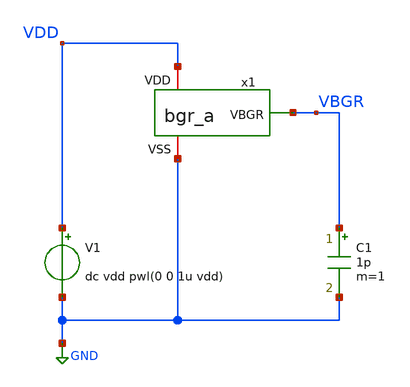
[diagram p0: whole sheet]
** sch_path: member_project/BGR/Maehashi/design/tb_bgr_a.sch
**.subckt tb_bgr_a
x1 VDD VBGR GND bgr_a
V1 VDD GND dc vdd pwl(0 0 1u vdd)
C1 VBGR GND 1p m=1
**** begin user architecture code


.option savecurrents
.temp 40
.param vdd = 5
.control
set units=degree
save all

alterparam vthMN = 0.1 ; Slow:0.1, Fast:-0.1
alterparam vthMP = 0.1 ; Slow:-0.1, Fast:0.1
alterparam magRS = 1 ; Slow:1.2, Fast:0.85
reset

op
show m
let vsat_marg_mp1 = @m.x1.xxmp1.m1[vds] - (@m.x1.xxmp1.m1[vgs] - @m.x1.xxmp1.m1[vth])
let vsat_marg_mp2 = @m.x1.xxmp2.m1[vds] - (@m.x1.xxmp2.m1[vgs] - @m.x1.xxmp2.m1[vth])
let vsat_marg_mp3 = @m.x1.xxmp3.m1[vds] - (@m.x1.xxmp3.m1[vgs] - @m.x1.xxmp3.m1[vth])
let vsat_marg_mp4 = @m.x1.xxmp4.m1[vds] - (@m.x1.xxmp4.m1[vgs] - @m.x1.xxmp4.m1[vth])
let vsat_marg_mp5 = @m.x1.xxmp5.m1[vds] - (@m.x1.xxmp5.m1[vgs] - @m.x1.xxmp5.m1[vth])
let vsat_marg_mp6 = @m.x1.xxmp6.m1[vds] - (@m.x1.xxmp6.m1[vgs] - @m.x1.xxmp6.m1[vth])

let vsat_marg_mn1 = @m.x1.xxmn1.m1[vds] - (@m.x1.xxmn1.m1[vgs] - @m.x1.xxmn1.m1[vth])
let vsat_marg_mn2 = @m.x1.xxmn2.m1[vds] - (@m.x1.xxmn2.m1[vgs] - @m.x1.xxmn2.m1[vth])
let vsat_marg_mn3 = @m.x1.xxmn3.m1[vds] - (@m.x1.xxmn3.m1[vgs] - @m.x1.xxmn3.m1[vth])
let vsat_marg_mn4 = @m.x1.xxmn4.m1[vds] - (@m.x1.xxmn4.m1[vgs] - @m.x1.xxmn4.m1[vth])

*echo '*** SF/5.0V/40deg ***' >> bgr_a_dcop.txt
*echo 'ignore VsatMargin Vds Vgs Vth' >> bgr_a_dcop.txt
*set appendwrite
*set wr_singlescale
*wrdata bgr_a_dcop.txt vsat_marg_mp1 @m.x1.xxmp1.m1[vds] @m.x1.xxmp1.m1[vgs] @m.x1.xxmp1.m1[vth]
*wrdata bgr_a_dcop.txt vsat_marg_mp2 @m.x1.xxmp2.m1[vds] @m.x1.xxmp2.m1[vgs] @m.x1.xxmp2.m1[vth]
*wrdata bgr_a_dcop.txt vsat_marg_mp3 @m.x1.xxmp3.m1[vds] @m.x1.xxmp3.m1[vgs] @m.x1.xxmp3.m1[vth]
*wrdata bgr_a_dcop.txt vsat_marg_mp4 @m.x1.xxmp4.m1[vds] @m.x1.xxmp4.m1[vgs] @m.x1.xxmp4.m1[vth]
*wrdata bgr_a_dcop.txt vsat_marg_mp5 @m.x1.xxmp5.m1[vds] @m.x1.xxmp5.m1[vgs] @m.x1.xxmp5.m1[vth]
*wrdata bgr_a_dcop.txt vsat_marg_mp6 @m.x1.xxmp6.m1[vds] @m.x1.xxmp6.m1[vgs] @m.x1.xxmp6.m1[vth]

*wrdata bgr_a_dcop.txt vsat_marg_mn1 @m.x1.xxmn1.m1[vds] @m.x1.xxmn1.m1[vgs] @m.x1.xxmn1.m1[vth]
*wrdata bgr_a_dcop.txt vsat_marg_mn2 @m.x1.xxmn2.m1[vds] @m.x1.xxmn2.m1[vgs] @m.x1.xxmn2.m1[vth]
*wrdata bgr_a_dcop.txt vsat_marg_mn3 @m.x1.xxmn3.m1[vds] @m.x1.xxmn3.m1[vgs] @m.x1.xxmn3.m1[vth]
*wrdata bgr_a_dcop.txt vsat_marg_mn4 @m.x1.xxmn4.m1[vds] @m.x1.xxmn4.m1[vgs] @m.x1.xxmn4.m1[vth]

.endc

 .include $::LIB/ip62_models
**** end user architecture code
**.ends
.GLOBAL GND
.end
